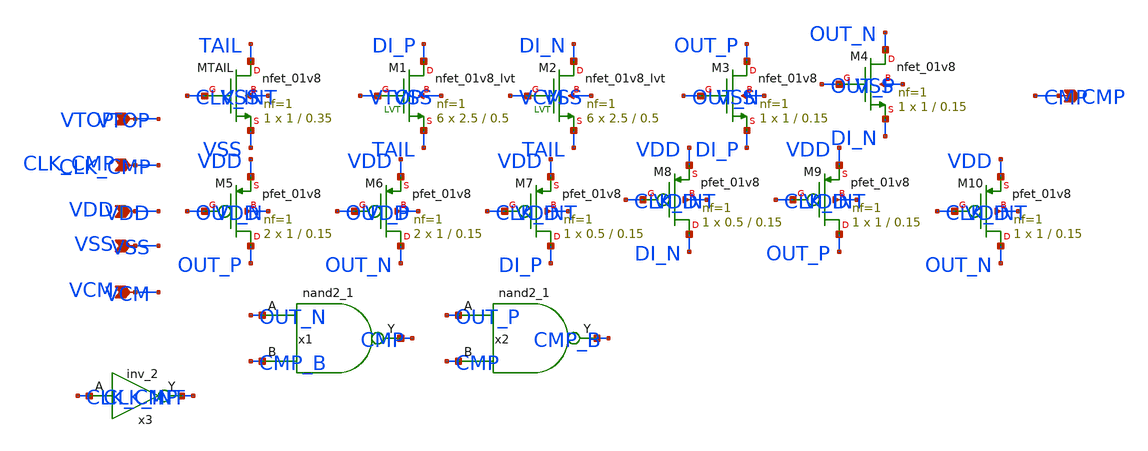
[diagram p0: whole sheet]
** sch_path: schematics/B2_comp/b2_comp_sa.sch
**.subckt b2_comp_sa VTOP VCM CLK_CMP VDD VSS CMP
*.ipin VTOP
*.ipin VCM
*.ipin CLK_CMP
*.ipin VDD
*.ipin VSS
*.opin CMP
XMTAIL TAIL CLK_INT VSS VSS sky130_fd_pr__nfet_01v8 L=0.35 W=1 nf=1 ad='int((1 + 1)/2) * 1 / 1 * 0.29'
+ as='int((1 + 2)/2) * 1 / 1 * 0.29' pd='2*int((1 + 1)/2) * (1 / 1 + 0.29)' ps='2*int((1 + 2)/2) * (1 / 1 + 0.29)'
+ nrd='0.29 / 1 ' nrs='0.29 / 1 ' sa=0 sb=0 sd=0 mult=1 m=1
XM1 DI_P VTOP TAIL VSS sky130_fd_pr__nfet_01v8_lvt L=0.5 W=2.5 nf=1 ad='int((1 + 1)/2) * 2.5 / 1 * 0.29'
+ as='int((1 + 2)/2) * 2.5 / 1 * 0.29' pd='2*int((1 + 1)/2) * (2.5 / 1 + 0.29)' ps='2*int((1 + 2)/2) * (2.5 / 1 + 0.29)'
+ nrd='0.29 / 2.5 ' nrs='0.29 / 2.5 ' sa=0 sb=0 sd=0 mult=6 m=6
XM2 DI_N VCM TAIL VSS sky130_fd_pr__nfet_01v8_lvt L=0.5 W=2.5 nf=1 ad='int((1 + 1)/2) * 2.5 / 1 * 0.29'
+ as='int((1 + 2)/2) * 2.5 / 1 * 0.29' pd='2*int((1 + 1)/2) * (2.5 / 1 + 0.29)' ps='2*int((1 + 2)/2) * (2.5 / 1 + 0.29)'
+ nrd='0.29 / 2.5 ' nrs='0.29 / 2.5 ' sa=0 sb=0 sd=0 mult=6 m=6
XM3 OUT_P OUT_N DI_P VSS sky130_fd_pr__nfet_01v8 L=0.15 W=1 nf=1 ad='int((1 + 1)/2) * 1 / 1 * 0.29' as='int((1 + 2)/2) * 1 / 1 * 0.29'
+ pd='2*int((1 + 1)/2) * (1 / 1 + 0.29)' ps='2*int((1 + 2)/2) * (1 / 1 + 0.29)' nrd='0.29 / 1 ' nrs='0.29 / 1 '
+ sa=0 sb=0 sd=0 mult=1 m=1
XM4 OUT_N OUT_P DI_N VSS sky130_fd_pr__nfet_01v8 L=0.15 W=1 nf=1 ad='int((1 + 1)/2) * 1 / 1 * 0.29' as='int((1 + 2)/2) * 1 / 1 * 0.29'
+ pd='2*int((1 + 1)/2) * (1 / 1 + 0.29)' ps='2*int((1 + 2)/2) * (1 / 1 + 0.29)' nrd='0.29 / 1 ' nrs='0.29 / 1 '
+ sa=0 sb=0 sd=0 mult=1 m=1
XM5 OUT_P OUT_N VDD VDD sky130_fd_pr__pfet_01v8 L=0.15 W=1 nf=1 ad='int((1 + 1)/2) * 1 / 1 * 0.29' as='int((1 + 2)/2) * 1 / 1 * 0.29'
+ pd='2*int((1 + 1)/2) * (1 / 1 + 0.29)' ps='2*int((1 + 2)/2) * (1 / 1 + 0.29)' nrd='0.29 / 1 ' nrs='0.29 / 1 '
+ sa=0 sb=0 sd=0 mult=2 m=2
XM6 OUT_N OUT_P VDD VDD sky130_fd_pr__pfet_01v8 L=0.15 W=1 nf=1 ad='int((1 + 1)/2) * 1 / 1 * 0.29' as='int((1 + 2)/2) * 1 / 1 * 0.29'
+ pd='2*int((1 + 1)/2) * (1 / 1 + 0.29)' ps='2*int((1 + 2)/2) * (1 / 1 + 0.29)' nrd='0.29 / 1 ' nrs='0.29 / 1 '
+ sa=0 sb=0 sd=0 mult=2 m=2
XM7 DI_P CLK_INT VDD VDD sky130_fd_pr__pfet_01v8 L=0.15 W=0.5 nf=1 ad='int((1 + 1)/2) * 0.5 / 1 * 0.29'
+ as='int((1 + 2)/2) * 0.5 / 1 * 0.29' pd='2*int((1 + 1)/2) * (0.5 / 1 + 0.29)' ps='2*int((1 + 2)/2) * (0.5 / 1 + 0.29)'
+ nrd='0.29 / 0.5 ' nrs='0.29 / 0.5 ' sa=0 sb=0 sd=0 mult=1 m=1
XM8 DI_N CLK_INT VDD VDD sky130_fd_pr__pfet_01v8 L=0.15 W=0.5 nf=1 ad='int((1 + 1)/2) * 0.5 / 1 * 0.29'
+ as='int((1 + 2)/2) * 0.5 / 1 * 0.29' pd='2*int((1 + 1)/2) * (0.5 / 1 + 0.29)' ps='2*int((1 + 2)/2) * (0.5 / 1 + 0.29)'
+ nrd='0.29 / 0.5 ' nrs='0.29 / 0.5 ' sa=0 sb=0 sd=0 mult=1 m=1
XM9 OUT_P CLK_INT VDD VDD sky130_fd_pr__pfet_01v8 L=0.15 W=1 nf=1 ad='int((1 + 1)/2) * 1 / 1 * 0.29'
+ as='int((1 + 2)/2) * 1 / 1 * 0.29' pd='2*int((1 + 1)/2) * (1 / 1 + 0.29)' ps='2*int((1 + 2)/2) * (1 / 1 + 0.29)'
+ nrd='0.29 / 1 ' nrs='0.29 / 1 ' sa=0 sb=0 sd=0 mult=1 m=1
XM10 OUT_N CLK_INT VDD VDD sky130_fd_pr__pfet_01v8 L=0.15 W=1 nf=1 ad='int((1 + 1)/2) * 1 / 1 * 0.29'
+ as='int((1 + 2)/2) * 1 / 1 * 0.29' pd='2*int((1 + 1)/2) * (1 / 1 + 0.29)' ps='2*int((1 + 2)/2) * (1 / 1 + 0.29)'
+ nrd='0.29 / 1 ' nrs='0.29 / 1 ' sa=0 sb=0 sd=0 mult=1 m=1
x1 OUT_N CMP_B VSS VSS VDD VDD CMP sky130_fd_sc_hd__nand2_1
x2 OUT_P CMP VSS VSS VDD VDD CMP_B sky130_fd_sc_hd__nand2_1
x3 CLK_CMP VSS VSS VDD VDD CLK_INT sky130_fd_sc_hd__inv_2
**.ends
.end
